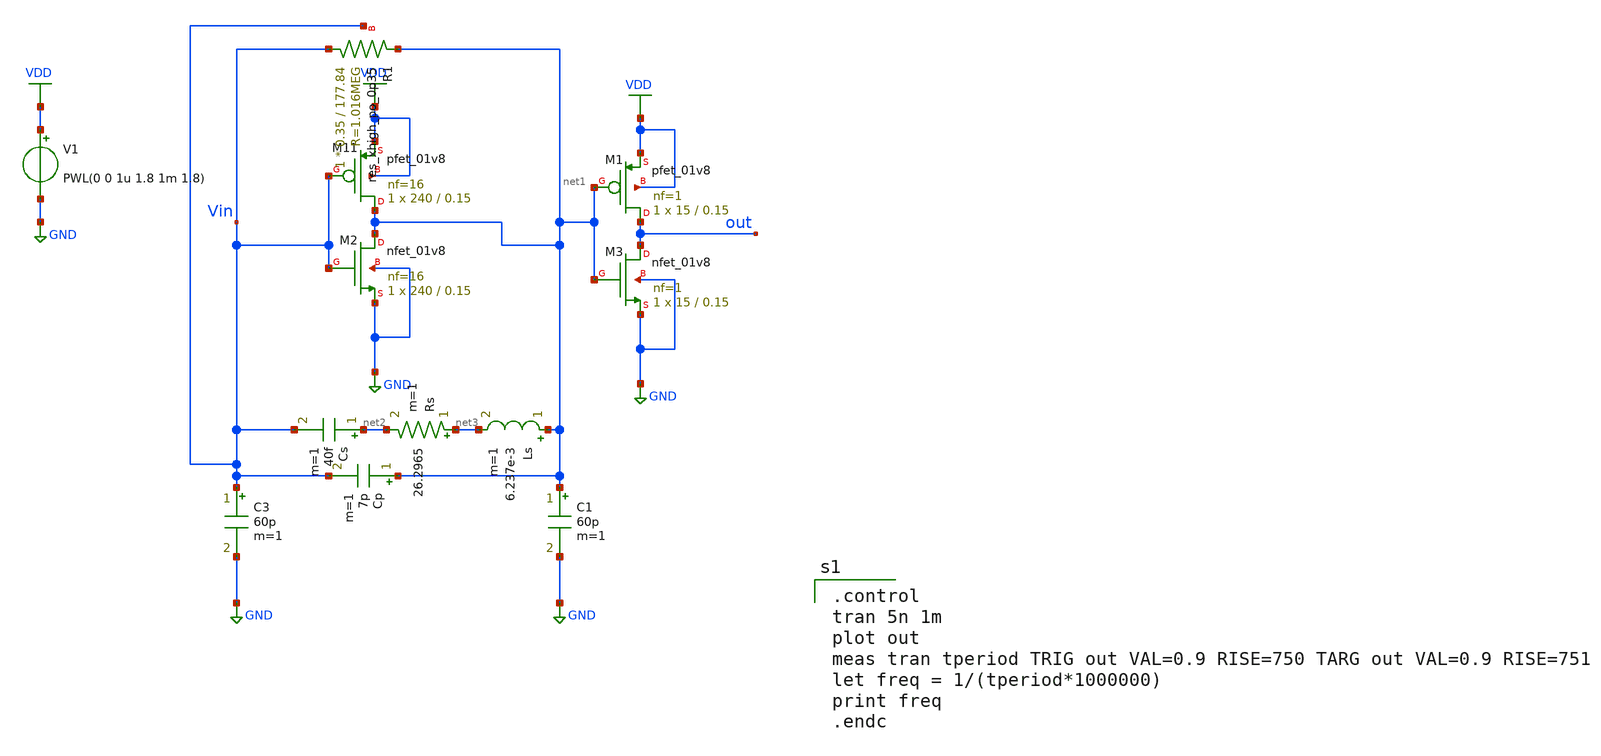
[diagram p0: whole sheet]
** sch_path: pll/xctl_lib/xctl/xschem/Crystal.sch
**.subckt Crystal
C1 net1 GND 60p m=1
C3 Vin GND 60p m=1
V1 VDD GND PWL(0 0 1u 1.8 1m 1.8)
Ls net1 net3 6.237e-3 m=1
Rs net3 net2 26.2965 m=1
Cs net2 Vin 40f m=1
Cp net1 Vin 7p m=1
XM11 net1 Vin VDD VDD sky130_fd_pr__pfet_01v8 L=0.15 W=240 nf=16 ad='int((nf+1)/2) * W/nf * 0.29' as='int((nf+2)/2) * W/nf * 0.29'
+ pd='2*int((nf+1)/2) * (W/nf + 0.29)' ps='2*int((nf+2)/2) * (W/nf + 0.29)' nrd='0.29 / W' nrs='0.29 / W'
+ sa=0 sb=0 sd=0 mult=1 m=1
XM2 net1 Vin GND GND sky130_fd_pr__nfet_01v8 L=0.15 W=240 nf=16 ad='int((16 + 1)/2) * 240 / 16 * 0.29'
+ as='int((16 + 2)/2) * 240 / 16 * 0.29' pd='2*int((16 + 1)/2) * (240 / 16 + 0.29)' ps='2*int((16 + 2)/2) * (240 / 16 + 0.29)'
+ nrd='0.29 / 240 ' nrs='0.29 / 240 ' sa=0 sb=0 sd=0 mult=1 m=1
XM1 out net1 VDD VDD sky130_fd_pr__pfet_01v8 L=0.15 W=15 nf=1 ad='int((nf+1)/2) * W/nf * 0.29' as='int((nf+2)/2) * W/nf * 0.29'
+ pd='2*int((nf+1)/2) * (W/nf + 0.29)' ps='2*int((nf+2)/2) * (W/nf + 0.29)' nrd='0.29 / W' nrs='0.29 / W'
+ sa=0 sb=0 sd=0 mult=1 m=1
XM3 out net1 GND GND sky130_fd_pr__nfet_01v8 L=0.15 W=15 nf=1 ad='int((1 + 1)/2) * 15 / 1 * 0.29' as='int((1 + 2)/2) * 15 / 1 * 0.29'
+ pd='2*int((1 + 1)/2) * (15 / 1 + 0.29)' ps='2*int((1 + 2)/2) * (15 / 1 + 0.29)' nrd='0.29 / 15 ' nrs='0.29 / 15 '
+ sa=0 sb=0 sd=0 mult=1 m=1
XR1 Vin net1 Vin sky130_fd_pr__res_xhigh_po_0p35 L=177.84 mult=1 m=1
**** begin user architecture code

** opencircuitdesign pdks install
.lib $::SKYWATER_MODELS/sky130.lib.spice tt



.control
tran 5n 1m
plot out
meas tran tperiod TRIG out VAL=0.9 RISE=750 TARG out VAL=0.9 RISE=751
let freq = 1/(tperiod*1000000)
print freq
.endc


**** end user architecture code
**.ends
.GLOBAL GND
.GLOBAL VDD
.end
